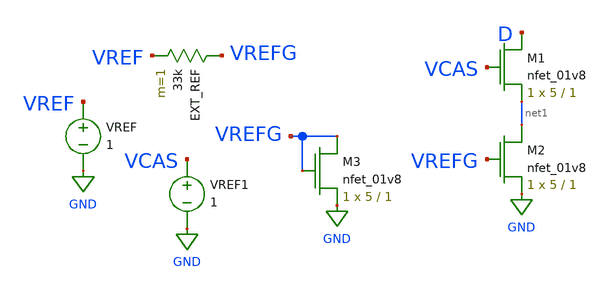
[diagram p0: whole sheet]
** sch_path: MP3/Schematics/iu_cell.sch
**.subckt iu_cell
XM1 D VCAS net1 GND sky130_fd_pr__nfet_01v8 L=1 W=5 nf=1 ad='int((nf+1)/2) * W/nf * 0.29' as='int((nf+2)/2) * W/nf * 0.29'
+ pd='2*int((nf+1)/2) * (W/nf + 0.29)' ps='2*int((nf+2)/2) * (W/nf + 0.29)' nrd='0.29 / W' nrs='0.29 / W'
+ sa=0 sb=0 sd=0 mult=1 m=1
XM2 net1 VREFG GND GND sky130_fd_pr__nfet_01v8 L=1 W=5 nf=1 ad='int((nf+1)/2) * W/nf * 0.29' as='int((nf+2)/2) * W/nf * 0.29'
+ pd='2*int((nf+1)/2) * (W/nf + 0.29)' ps='2*int((nf+2)/2) * (W/nf + 0.29)' nrd='0.29 / W' nrs='0.29 / W'
+ sa=0 sb=0 sd=0 mult=1 m=1
XM3 VREFG VREFG GND GND sky130_fd_pr__nfet_01v8 L=1 W=5 nf=1 ad='int((nf+1)/2) * W/nf * 0.29' as='int((nf+2)/2) * W/nf * 0.29'
+ pd='2*int((nf+1)/2) * (W/nf + 0.29)' ps='2*int((nf+2)/2) * (W/nf + 0.29)' nrd='0.29 / W' nrs='0.29 / W'
+ sa=0 sb=0 sd=0 mult=1 m=1
EXT_REF VREFG VREF 33k m=1
VREF VREF GND 1
VREF1 VCAS GND 1
**.ends
.GLOBAL GND
.end
